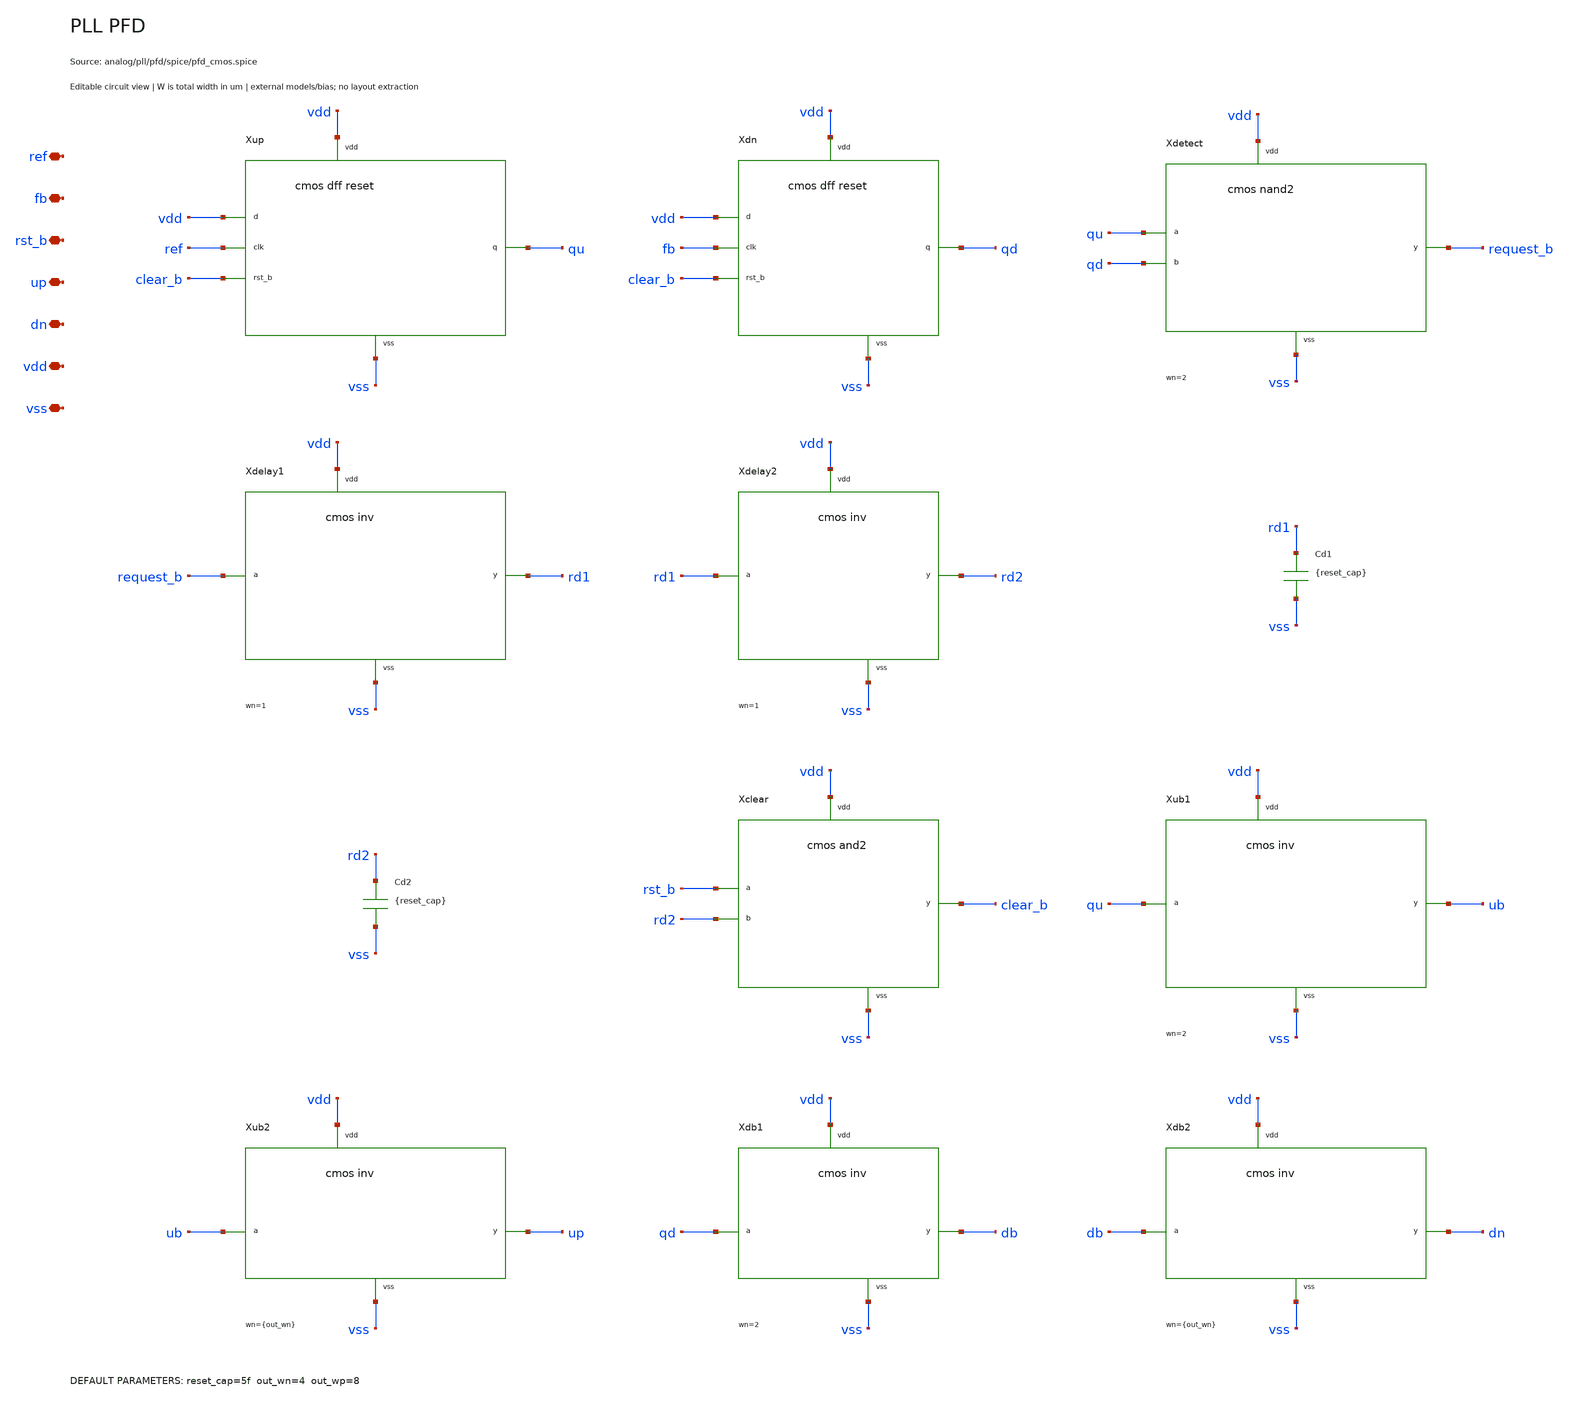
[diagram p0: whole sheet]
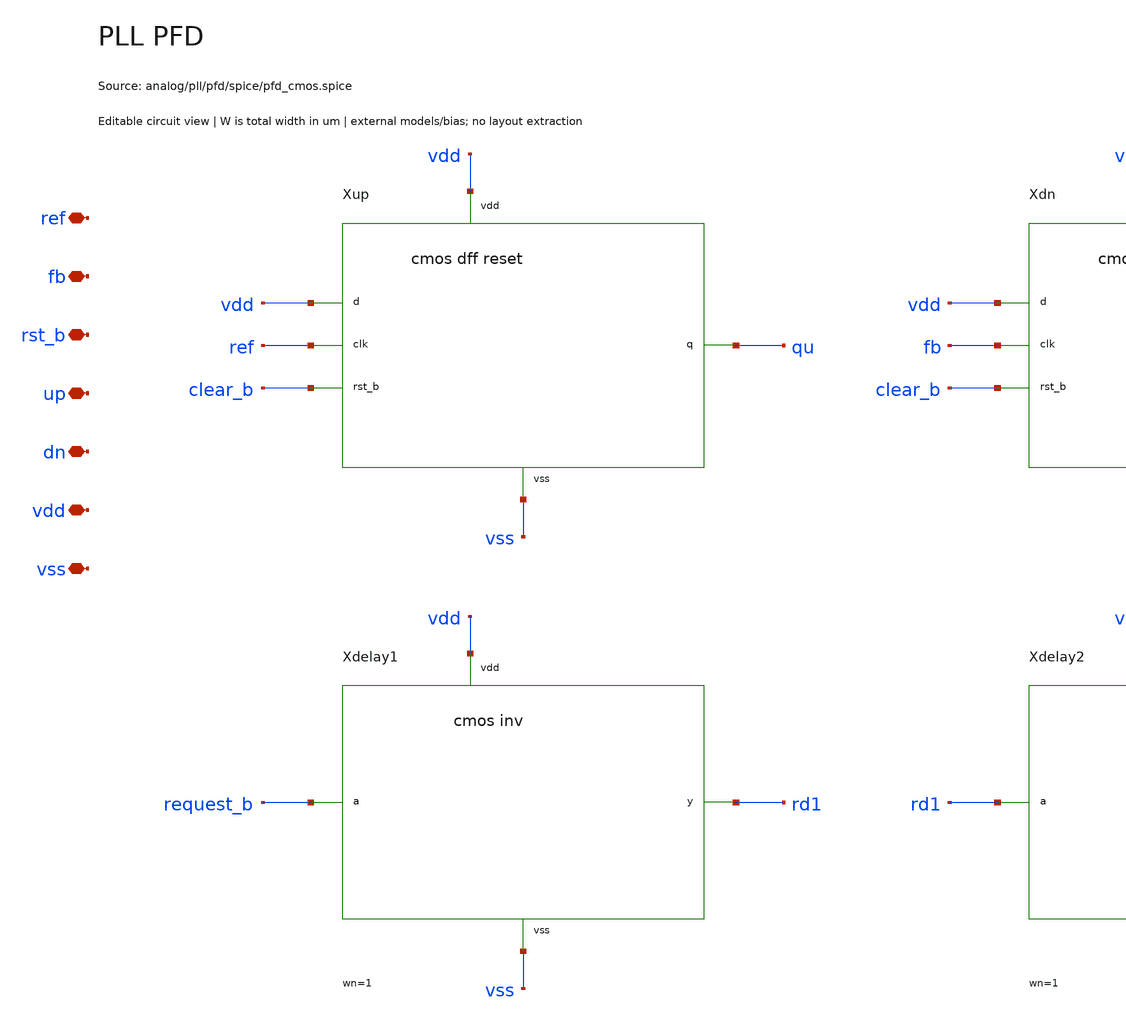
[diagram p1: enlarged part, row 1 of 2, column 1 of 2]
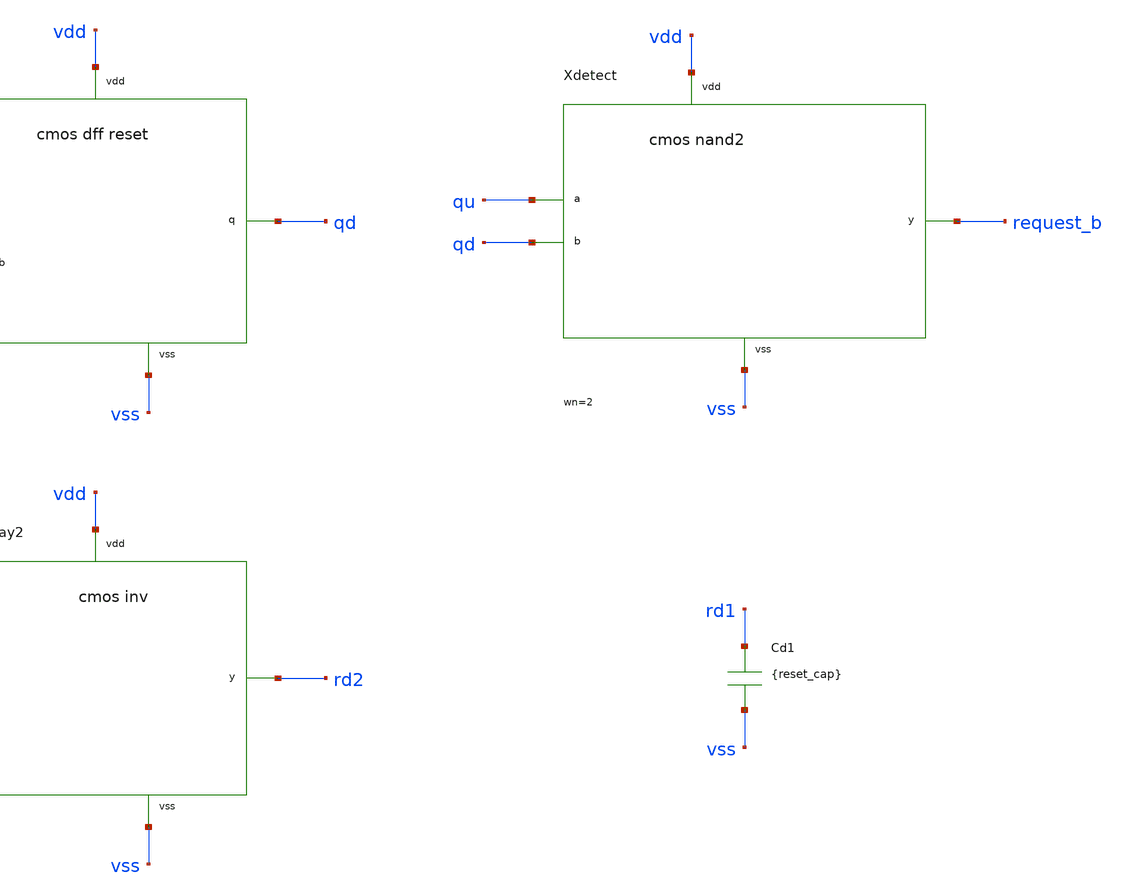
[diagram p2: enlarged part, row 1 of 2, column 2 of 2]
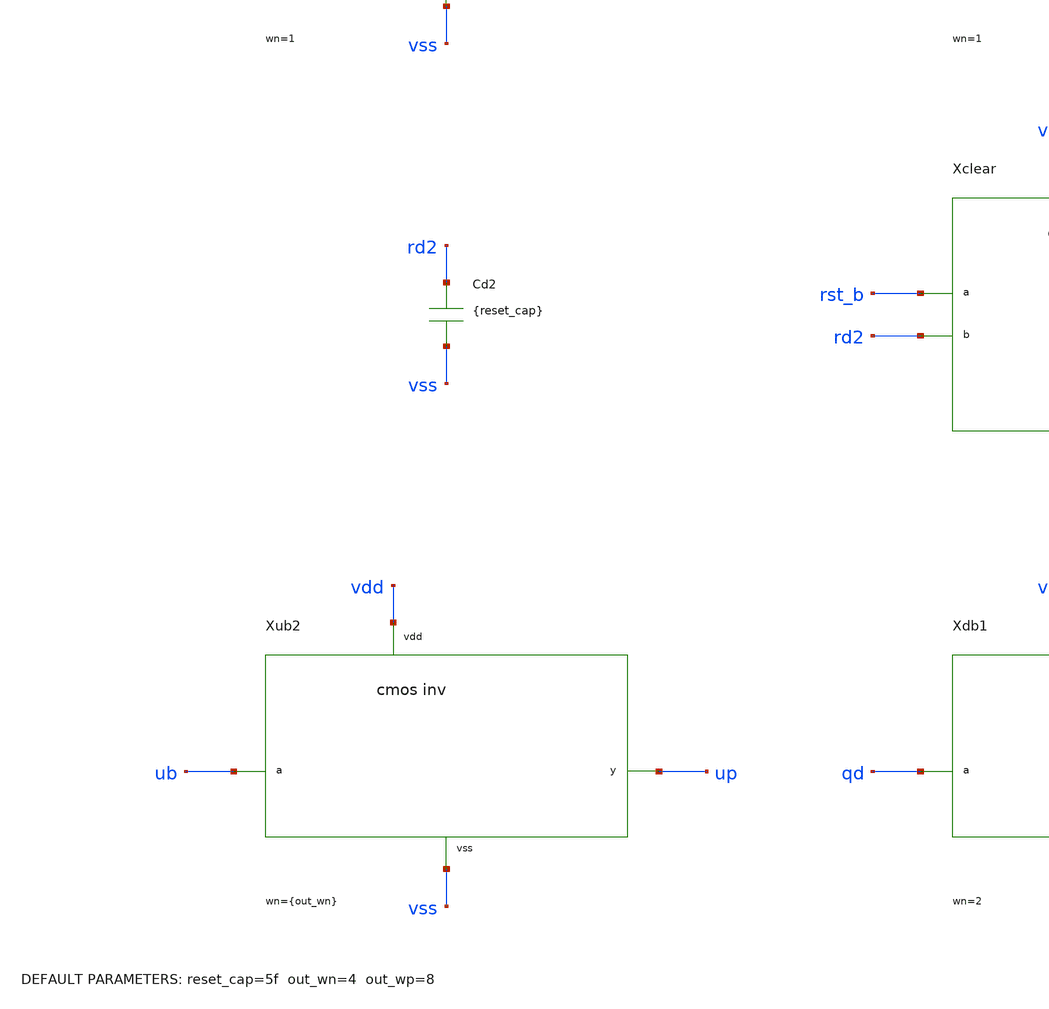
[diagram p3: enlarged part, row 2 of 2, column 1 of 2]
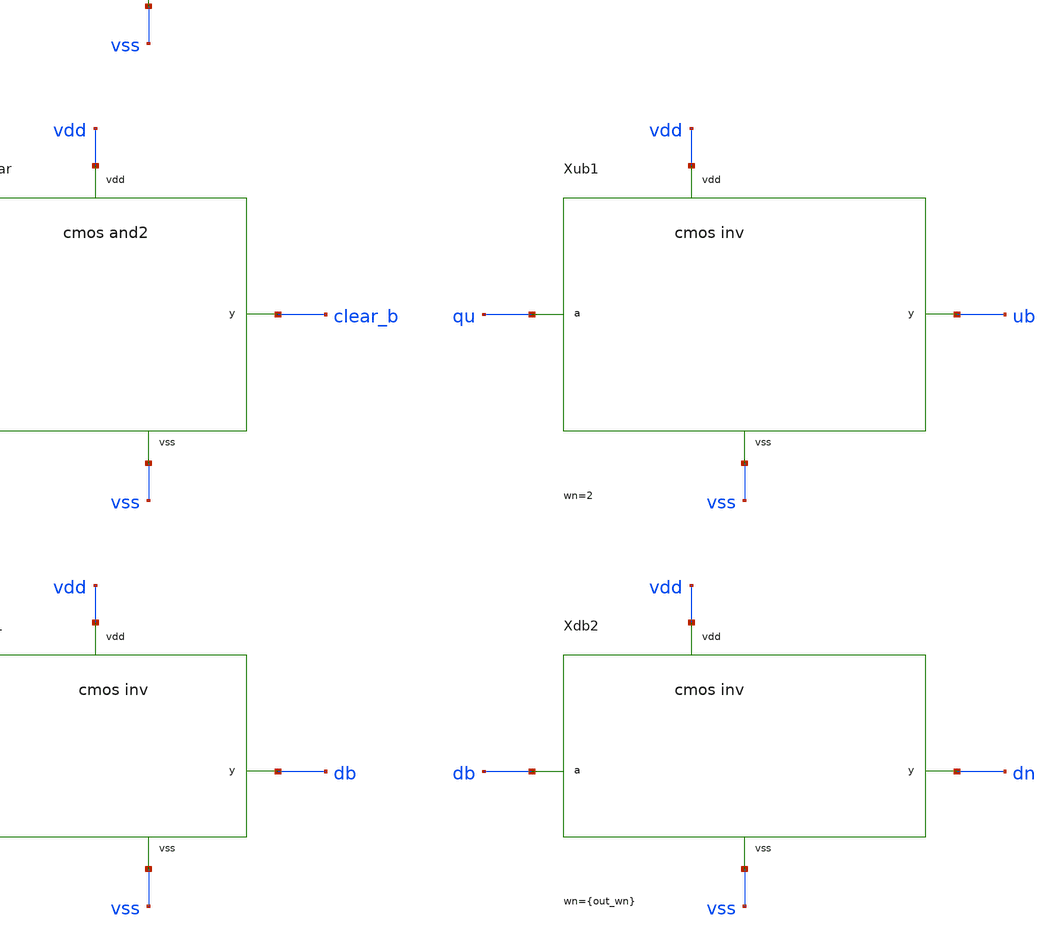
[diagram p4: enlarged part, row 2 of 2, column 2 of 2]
** sch_path: analog/pll/pfd/schematic/pll_pfd.sch
**.subckt pll_pfd ref fb rst_b up dn vdd vss
*.iopin ref
*.iopin fb
*.iopin rst_b
*.iopin up
*.iopin dn
*.iopin vdd
*.iopin vss
Xup vdd ref clear_b qu vdd vss pll_cmos_dff_reset
Xdn vdd fb clear_b qd vdd vss pll_cmos_dff_reset
Xdetect qu qd request_b vdd vss serdes_cmos_nand2 wn=2 wp=2
Xdelay1 request_b rd1 vdd vss serdes_cmos_inv wn=1 wp=2
Xdelay2 rd1 rd2 vdd vss serdes_cmos_inv wn=1 wp=2
Cd1 rd1 vss {reset_cap}
Cd2 rd2 vss {reset_cap}
Xclear rst_b rd2 clear_b vdd vss serdes_cmos_and2
Xub1 qu ub vdd vss serdes_cmos_inv wn=2 wp=4
Xub2 ub up vdd vss serdes_cmos_inv wn={out_wn} wp={out_wp}
Xdb1 qd db vdd vss serdes_cmos_inv wn=2 wp=4
Xdb2 db dn vdd vss serdes_cmos_inv wn={out_wn} wp={out_wp}
**.ends
.end
